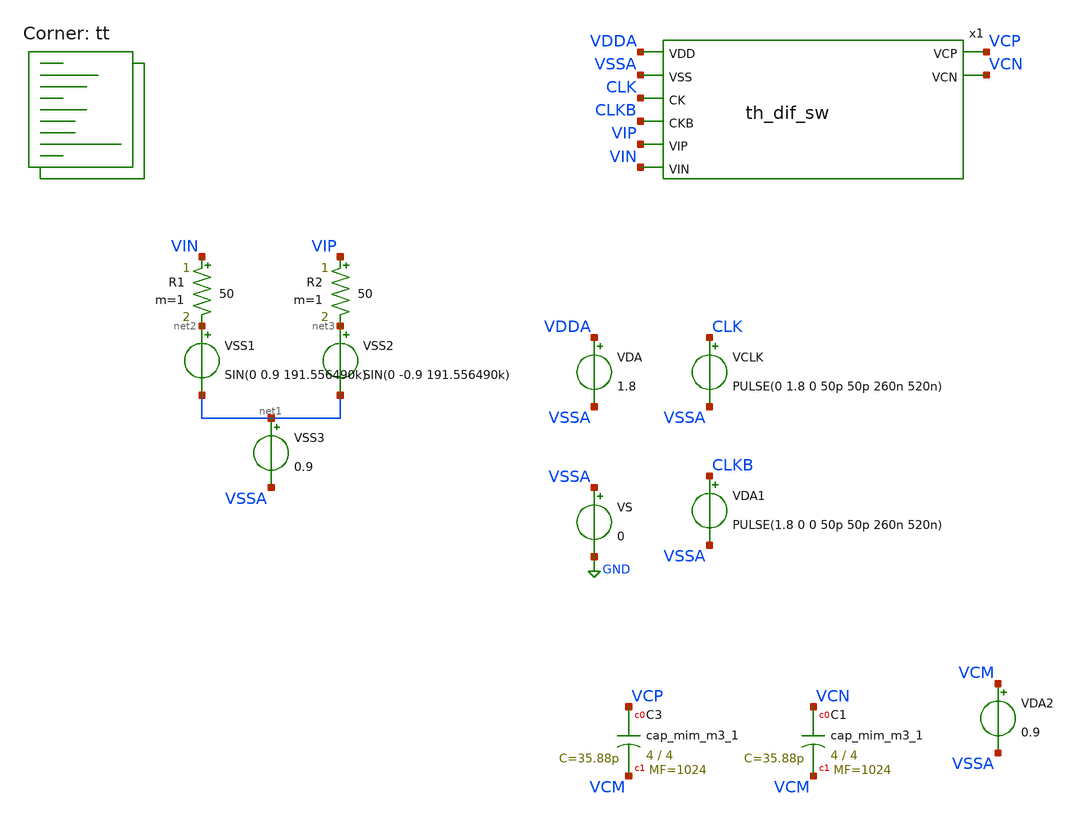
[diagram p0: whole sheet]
** sch_path: xschem/th_tb.sch
**.subckt th_tb
VS VSSA GND 0
VDA VDDA VSSA 1.8
VSS1 net2 net1 SIN(0 0.9 191.556490k)
VSS2 net3 net1 SIN(0 -0.9 191.556490k)
VSS3 net1 VSSA 0.9
VCLK CLK VSSA PULSE(0 1.8 0 50p 50p 260n 520n)
R1 VIN net2 50 m=1
R2 VIP net3 50 m=1
VDA1 CLKB VSSA PULSE(1.8 0 0 50p 50p 260n 520n)
x1 VDDA VSSA CLK CLKB VIP VIN VCP VCN th_dif_sw
VDA2 VCM VSSA 0.9
XC3 VCP VCM sky130_fd_pr__cap_mim_m3_1 W=4 L=4 MF=1024 m=1024
XC1 VCN VCM sky130_fd_pr__cap_mim_m3_1 W=4 L=4 MF=1024 m=1024
**** begin user architecture code

** opencircuitdesign pdks install
* .lib $::SKYWATER_MODELS/sky130.lib.spice tt
.include $PDK_ROOT/$PDK/libs.ref/sky130_fd_sc_hd/spice/sky130_fd_sc_hd.spice



.option wnflag=0 bypass=1
.options method=trap rawfile=binary
.options solver=klu nomod
.control
set num_threads=6
save CLK CLKB VIP VIN VCP VCN
global netlist_dir .
set wr_singlescale
tran 1n 535u  ; Mengubah start time menjadi 1n
remzerovec
write th_tb.raw
wrdata th_tb.txt CLK CLKB VIP VIN VCP VCN
quit 0
.endc

.lib $::SKYWATER_MODELS/sky130.lib.spice tt
**** end user architecture code
**.ends

* expanding   symbol:  th_dif_sw.sym # of pins=8
** sym_path: th_dif_sw.sym
** sch_path: th_dif_sw.sch
.subckt th_dif_sw VDD VSS CK CKB VIP VIN VCP VCN
*.ipin VDD
*.ipin VSS
*.ipin CK
*.ipin CKB
*.ipin VIP
*.ipin VIN
*.opin VCP
*.opin VCN
x1 VDD VSS CK_BUFF CKB_BUFF VIP VCP th_sw
x2 VDD VSS CK_BUFF CKB_BUFF VIN VCN th_sw
x3 CK VSS VSS VDD VDD CK_BUFF sky130_fd_sc_hs__buf_16
x4 CKB VSS VSS VDD VDD CKB_BUFF sky130_fd_sc_hs__buf_16
.ends


* expanding   symbol:  th_sw.sym # of pins=6
** sym_path: th_sw.sym
** sch_path: th_sw.sch
.subckt th_sw VDD VSS CK CKB IN OUT
*.ipin VDD
*.ipin VSS
*.ipin CK
*.ipin CKB
*.ipin IN
*.opin OUT
x1 VDD VSS CK VGS IN OUT th_sw_main
x2 VDD VSS CK CKB IN VGS bootstrap
.ends


* expanding   symbol:  th_sw_main.sym # of pins=6
** sym_path: xschem/th_sw_main.sym
** sch_path: xschem/th_sw_main.sch
.subckt th_sw_main VDD VSS CK VGS IN OUT
*.ipin VDD
*.ipin VSS
*.ipin CK
*.ipin VGS
*.ipin IN
*.opin OUT
XM10 IN CK IN VSS sky130_fd_pr__nfet_01v8 L=0.15 W=20 nf=1 ad='int((nf+1)/2) * W/nf * 0.29' as='int((nf+2)/2) * W/nf * 0.29'
+ pd='2*int((nf+1)/2) * (W/nf + 0.29)' ps='2*int((nf+2)/2) * (W/nf + 0.29)' nrd='0.29 / W' nrs='0.29 / W'
+ sa=0 sb=0 sd=0 mult=1 m=1
XM11 OUT VGS IN VSS sky130_fd_pr__nfet_01v8 L=0.15 W=20 nf=1 ad='int((nf+1)/2) * W/nf * 0.29' as='int((nf+2)/2) * W/nf * 0.29'
+ pd='2*int((nf+1)/2) * (W/nf + 0.29)' ps='2*int((nf+2)/2) * (W/nf + 0.29)' nrd='0.29 / W' nrs='0.29 / W'
+ sa=0 sb=0 sd=0 mult=1 m=1
XM12 OUT CK OUT VSS sky130_fd_pr__nfet_01v8 L=0.15 W=20 nf=1 ad='int((nf+1)/2) * W/nf * 0.29' as='int((nf+2)/2) * W/nf * 0.29'
+ pd='2*int((nf+1)/2) * (W/nf + 0.29)' ps='2*int((nf+2)/2) * (W/nf + 0.29)' nrd='0.29 / W' nrs='0.29 / W'
+ sa=0 sb=0 sd=0 mult=1 m=1
.ends


* expanding   symbol:  bootstrap.sym # of pins=6
** sym_path: xschem/bootstrap.sym
** sch_path: xschem/bootstrap.sch
.subckt bootstrap VDD VSS CK CKB IN VGS
*.ipin VDD
*.ipin VSS
*.ipin CK
*.ipin CKB
*.ipin IN
*.opin VGS
XM1 net1 CKB VDD VDD sky130_fd_pr__pfet_01v8 L=0.15 W=0.75 nf=1 ad='int((nf+1)/2) * W/nf * 0.29' as='int((nf+2)/2) * W/nf * 0.29'
+ pd='2*int((nf+1)/2) * (W/nf + 0.29)' ps='2*int((nf+2)/2) * (W/nf + 0.29)' nrd='0.29 / W' nrs='0.29 / W'
+ sa=0 sb=0 sd=0 mult=1 m=1
XM2 net2 VGS VDD net2 sky130_fd_pr__pfet_01v8 L=0.15 W=4 nf=1 ad='int((nf+1)/2) * W/nf * 0.29' as='int((nf+2)/2) * W/nf * 0.29'
+ pd='2*int((nf+1)/2) * (W/nf + 0.29)' ps='2*int((nf+2)/2) * (W/nf + 0.29)' nrd='0.29 / W' nrs='0.29 / W'
+ sa=0 sb=0 sd=0 mult=1 m=1
XM3 VGS net1 net2 net2 sky130_fd_pr__pfet_01v8 L=0.15 W=2 nf=1 ad='int((nf+1)/2) * W/nf * 0.29' as='int((nf+2)/2) * W/nf * 0.29'
+ pd='2*int((nf+1)/2) * (W/nf + 0.29)' ps='2*int((nf+2)/2) * (W/nf + 0.29)' nrd='0.29 / W' nrs='0.29 / W'
+ sa=0 sb=0 sd=0 mult=1 m=1
XM4 net1 CKB net4 VSS sky130_fd_pr__nfet_01v8 L=0.15 W=0.5 nf=1 ad='int((nf+1)/2) * W/nf * 0.29' as='int((nf+2)/2) * W/nf * 0.29'
+ pd='2*int((nf+1)/2) * (W/nf + 0.29)' ps='2*int((nf+2)/2) * (W/nf + 0.29)' nrd='0.29 / W' nrs='0.29 / W'
+ sa=0 sb=0 sd=0 mult=1 m=1
XM5 net4 CK VSS VSS sky130_fd_pr__nfet_01v8 L=0.15 W=2 nf=1 ad='int((nf+1)/2) * W/nf * 0.29' as='int((nf+2)/2) * W/nf * 0.29'
+ pd='2*int((nf+1)/2) * (W/nf + 0.29)' ps='2*int((nf+2)/2) * (W/nf + 0.29)' nrd='0.29 / W' nrs='0.29 / W'
+ sa=0 sb=0 sd=0 mult=1 m=1
XM6 net1 VGS net4 VSS sky130_fd_pr__nfet_01v8 L=0.15 W=4 nf=1 ad='int((nf+1)/2) * W/nf * 0.29' as='int((nf+2)/2) * W/nf * 0.29'
+ pd='2*int((nf+1)/2) * (W/nf + 0.29)' ps='2*int((nf+2)/2) * (W/nf + 0.29)' nrd='0.29 / W' nrs='0.29 / W'
+ sa=0 sb=0 sd=0 mult=1 m=1
XM7 IN VGS net4 VSS sky130_fd_pr__nfet_01v8 L=0.15 W=4 nf=1 ad='int((nf+1)/2) * W/nf * 0.29' as='int((nf+2)/2) * W/nf * 0.29'
+ pd='2*int((nf+1)/2) * (W/nf + 0.29)' ps='2*int((nf+2)/2) * (W/nf + 0.29)' nrd='0.29 / W' nrs='0.29 / W'
+ sa=0 sb=0 sd=0 mult=1 m=1
XM8 VGS VDD net3 VSS sky130_fd_pr__nfet_01v8 L=0.15 W=7.5 nf=1 ad='int((nf+1)/2) * W/nf * 0.29' as='int((nf+2)/2) * W/nf * 0.29'
+ pd='2*int((nf+1)/2) * (W/nf + 0.29)' ps='2*int((nf+2)/2) * (W/nf + 0.29)' nrd='0.29 / W' nrs='0.29 / W'
+ sa=0 sb=0 sd=0 mult=1 m=1
XM9 net3 CK VSS VSS sky130_fd_pr__nfet_01v8 L=0.15 W=7.5 nf=1 ad='int((nf+1)/2) * W/nf * 0.29' as='int((nf+2)/2) * W/nf * 0.29'
+ pd='2*int((nf+1)/2) * (W/nf + 0.29)' ps='2*int((nf+2)/2) * (W/nf + 0.29)' nrd='0.29 / W' nrs='0.29 / W'
+ sa=0 sb=0 sd=0 mult=1 m=1
XC1 net2 net4 sky130_fd_pr__cap_mim_m3_1 W=4 L=4 MF=32 m=32
.ends

.GLOBAL GND
.end
